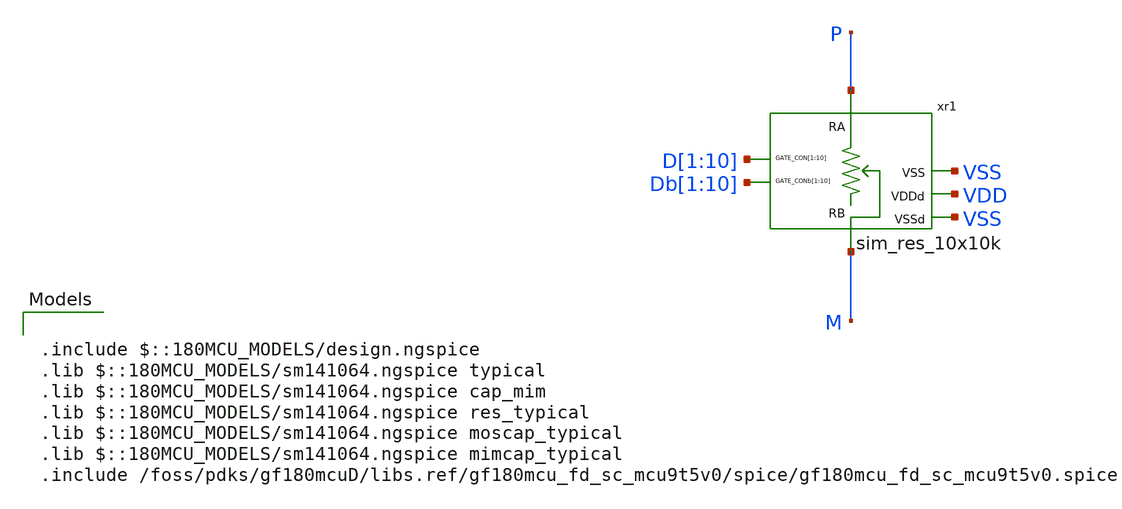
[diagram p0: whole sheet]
** sch_path: designs/libs/tb_passive_array/tb_res_10x10k.sch
**.subckt tb_res_10x10k
xr1 D[1] D[2] D[3] D[4] D[5] D[6] D[7] D[8] D[9] D[10] Db[1] Db[2] Db[3] Db[4] Db[5] Db[6] Db[7]
+ Db[8] Db[9] Db[10] P M VSS VDD VSS sim_res_10x10k
**** begin user architecture code


vd[1] d[1] 0 dc 0
vd[2] d[2] 0 dc 0
vd[3] d[3] 0 dc 0
vd[4] d[4] 0 dc 0
vd[5] d[5] 0 dc 0

vd[6] d[6] 0 dc 0
vd[7] d[7] 0 dc 0
vd[8] d[8] 0 dc 0
vd[9] d[9] 0 dc 0
vd[10] d[10] 0 dc 0

vdb[1] db[1] 0 dc 3.3
vdb[2] db[2] 0 dc 3.3
vdb[3] db[3] 0 dc 3.3
vdb[4] db[4] 0 dc 3.3
vdb[5] db[5] 0 dc 3.3

vdb[6] db[6] 0 dc 3.3
vdb[7] db[7] 0 dc 3.3
vdb[8] db[8] 0 dc 3.3
vdb[9] db[9] 0 dc 3.3
vdb[10] db[10] 0 dc 3.3

vvdd VDD 0 dc 3.3
vvss VSS 0 dc 0

vp p 0 0
vm m 0 0

.control
alter vd[1] = 3.3
alter vdb[1] = 0
save all
dc vp 0 3.3 0.01
write tb_res_10x10k.raw
set appendwrite

reset
alter vd[2] = 3.3
alter vdb[2] = 0
save all
dc vp 0 3.3 0.01
write tb_res_10x10k.raw

reset
alter vd[3] = 3.3
alter vdb[3] = 0
save all
dc vp 0 3.3 0.01
write tb_res_10x10k.raw

reset
alter vd[4] = 3.3
alter vdb[4] = 0
save all
dc vp 0 3.3 0.01
write tb_res_10x10k.raw

reset
alter vd[5] = 3.3
alter vdb[5] = 0
save all
dc vp 0 3.3 0.01
write tb_res_10x10k.raw

reset
alter vd[6] = 3.3
alter vdb[6] = 0
save all
dc vp 0 3.3 0.01
write tb_res_10x10k.raw

reset
alter vd[7] = 3.3
alter vdb[7] = 0
save all
dc vp 0 3.3 0.01
write tb_res_10x10k.raw

reset
alter vd[8] = 3.3
alter vdb[8] = 0
save all
dc vp 0 3.3 0.01
write tb_res_10x10k.raw

reset
alter vd[9] = 3.3
alter vdb[9] = 0
save all
dc vp 0 3.3 0.01
write tb_res_10x10k.raw

reset
alter vd[10] = 3.3
alter vdb[10] = 0
save all
dc vp 0 3.3 0.01
write tb_res_10x10k.raw
.endc



.include $::180MCU_MODELS/design.ngspice
.lib $::180MCU_MODELS/sm141064.ngspice typical
.lib $::180MCU_MODELS/sm141064.ngspice cap_mim
.lib $::180MCU_MODELS/sm141064.ngspice res_typical
.lib $::180MCU_MODELS/sm141064.ngspice moscap_typical
.lib $::180MCU_MODELS/sm141064.ngspice mimcap_typical
.include /foss/pdks/gf180mcuD/libs.ref/gf180mcu_fd_sc_mcu9t5v0/spice/gf180mcu_fd_sc_mcu9t5v0.spice

**** end user architecture code
**.ends
.end
